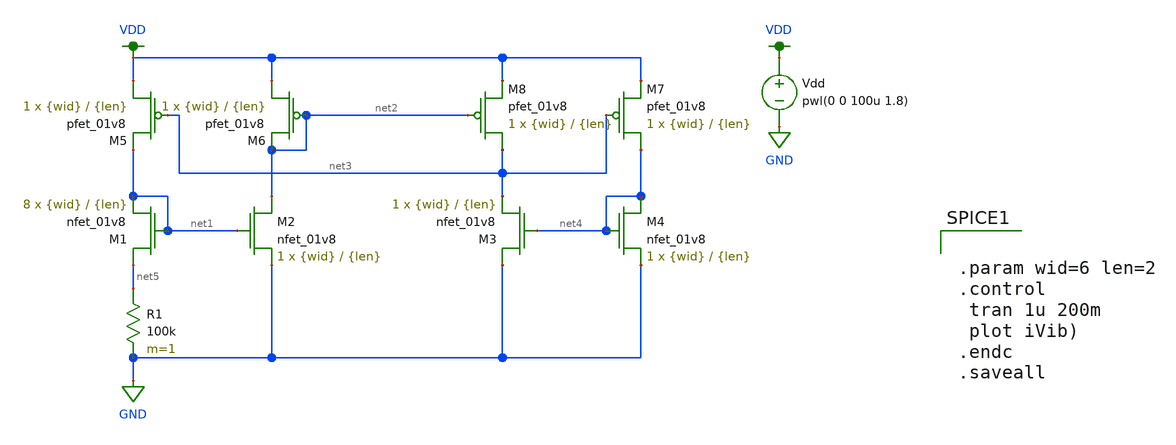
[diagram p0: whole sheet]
** sch_path: MADVLSI_MP3/BiasGenTransSim.sch
**.subckt BiasGenTransSim
XM1 net5 net1 net1 GND sky130_fd_pr__nfet_01v8 L={len} W={wid} nf=1 ad='int((nf+1)/2) * W/nf * 0.29'
+ as='int((nf+2)/2) * W/nf * 0.29' pd='2*int((nf+1)/2) * (W/nf + 0.29)' ps='2*int((nf+2)/2) * (W/nf + 0.29)'
+ nrd='0.29 / W' nrs='0.29 / W' sa=0 sb=0 sd=0 mult=8 m=8
XM6 VDD net2 net2 VDD sky130_fd_pr__pfet_01v8 L={len} W={wid} nf=1 ad='int((nf+1)/2) * W/nf * 0.29' as='int((nf+2)/2) * W/nf * 0.29'
+ pd='2*int((nf+1)/2) * (W/nf + 0.29)' ps='2*int((nf+2)/2) * (W/nf + 0.29)' nrd='0.29 / W' nrs='0.29 / W'
+ sa=0 sb=0 sd=0 mult=1 m=1
XM2 net2 net1 GND GND sky130_fd_pr__nfet_01v8 L={len} W={wid} nf=1 ad='int((nf+1)/2) * W/nf * 0.29' as='int((nf+2)/2) * W/nf * 0.29'
+ pd='2*int((nf+1)/2) * (W/nf + 0.29)' ps='2*int((nf+2)/2) * (W/nf + 0.29)' nrd='0.29 / W' nrs='0.29 / W'
+ sa=0 sb=0 sd=0 mult=1 m=1
XM3 GND net4 net3 GND sky130_fd_pr__nfet_01v8 L={len} W={wid} nf=1 ad='int((nf+1)/2) * W/nf * 0.29' as='int((nf+2)/2) * W/nf * 0.29'
+ pd='2*int((nf+1)/2) * (W/nf + 0.29)' ps='2*int((nf+2)/2) * (W/nf + 0.29)' nrd='0.29 / W' nrs='0.29 / W'
+ sa=0 sb=0 sd=0 mult=1 m=1
XM4 net4 net4 GND GND sky130_fd_pr__nfet_01v8 L={len} W={wid} nf=1 ad='int((nf+1)/2) * W/nf * 0.29' as='int((nf+2)/2) * W/nf * 0.29'
+ pd='2*int((nf+1)/2) * (W/nf + 0.29)' ps='2*int((nf+2)/2) * (W/nf + 0.29)' nrd='0.29 / W' nrs='0.29 / W'
+ sa=0 sb=0 sd=0 mult=1 m=1
XM5 VDD net3 net1 VDD sky130_fd_pr__pfet_01v8 L={len} W={wid} nf=1 ad='int((nf+1)/2) * W/nf * 0.29' as='int((nf+2)/2) * W/nf * 0.29'
+ pd='2*int((nf+1)/2) * (W/nf + 0.29)' ps='2*int((nf+2)/2) * (W/nf + 0.29)' nrd='0.29 / W' nrs='0.29 / W'
+ sa=0 sb=0 sd=0 mult=1 m=1
XM7 net4 net3 VDD VDD sky130_fd_pr__pfet_01v8 L={len} W={wid} nf=1 ad='int((nf+1)/2) * W/nf * 0.29' as='int((nf+2)/2) * W/nf * 0.29'
+ pd='2*int((nf+1)/2) * (W/nf + 0.29)' ps='2*int((nf+2)/2) * (W/nf + 0.29)' nrd='0.29 / W' nrs='0.29 / W'
+ sa=0 sb=0 sd=0 mult=1 m=1
XM8 net3 net2 VDD VDD sky130_fd_pr__pfet_01v8 L={len} W={wid} nf=1 ad='int((nf+1)/2) * W/nf * 0.29' as='int((nf+2)/2) * W/nf * 0.29'
+ pd='2*int((nf+1)/2) * (W/nf + 0.29)' ps='2*int((nf+2)/2) * (W/nf + 0.29)' nrd='0.29 / W' nrs='0.29 / W'
+ sa=0 sb=0 sd=0 mult=1 m=1
R1 net5 GND 100k m=1
Vdd VDD GND pwl(0 0 100u 1.8)
**** begin user architecture code

.lib $::SKYWATER_MODELS/sky130.lib.spice tt



.param wid=6 len=2
.control
 tran 1u 200m
 plot iVib)
.endc
.saveall

**** end user architecture code
**.ends
.GLOBAL VDD
.GLOBAL GND
.end
